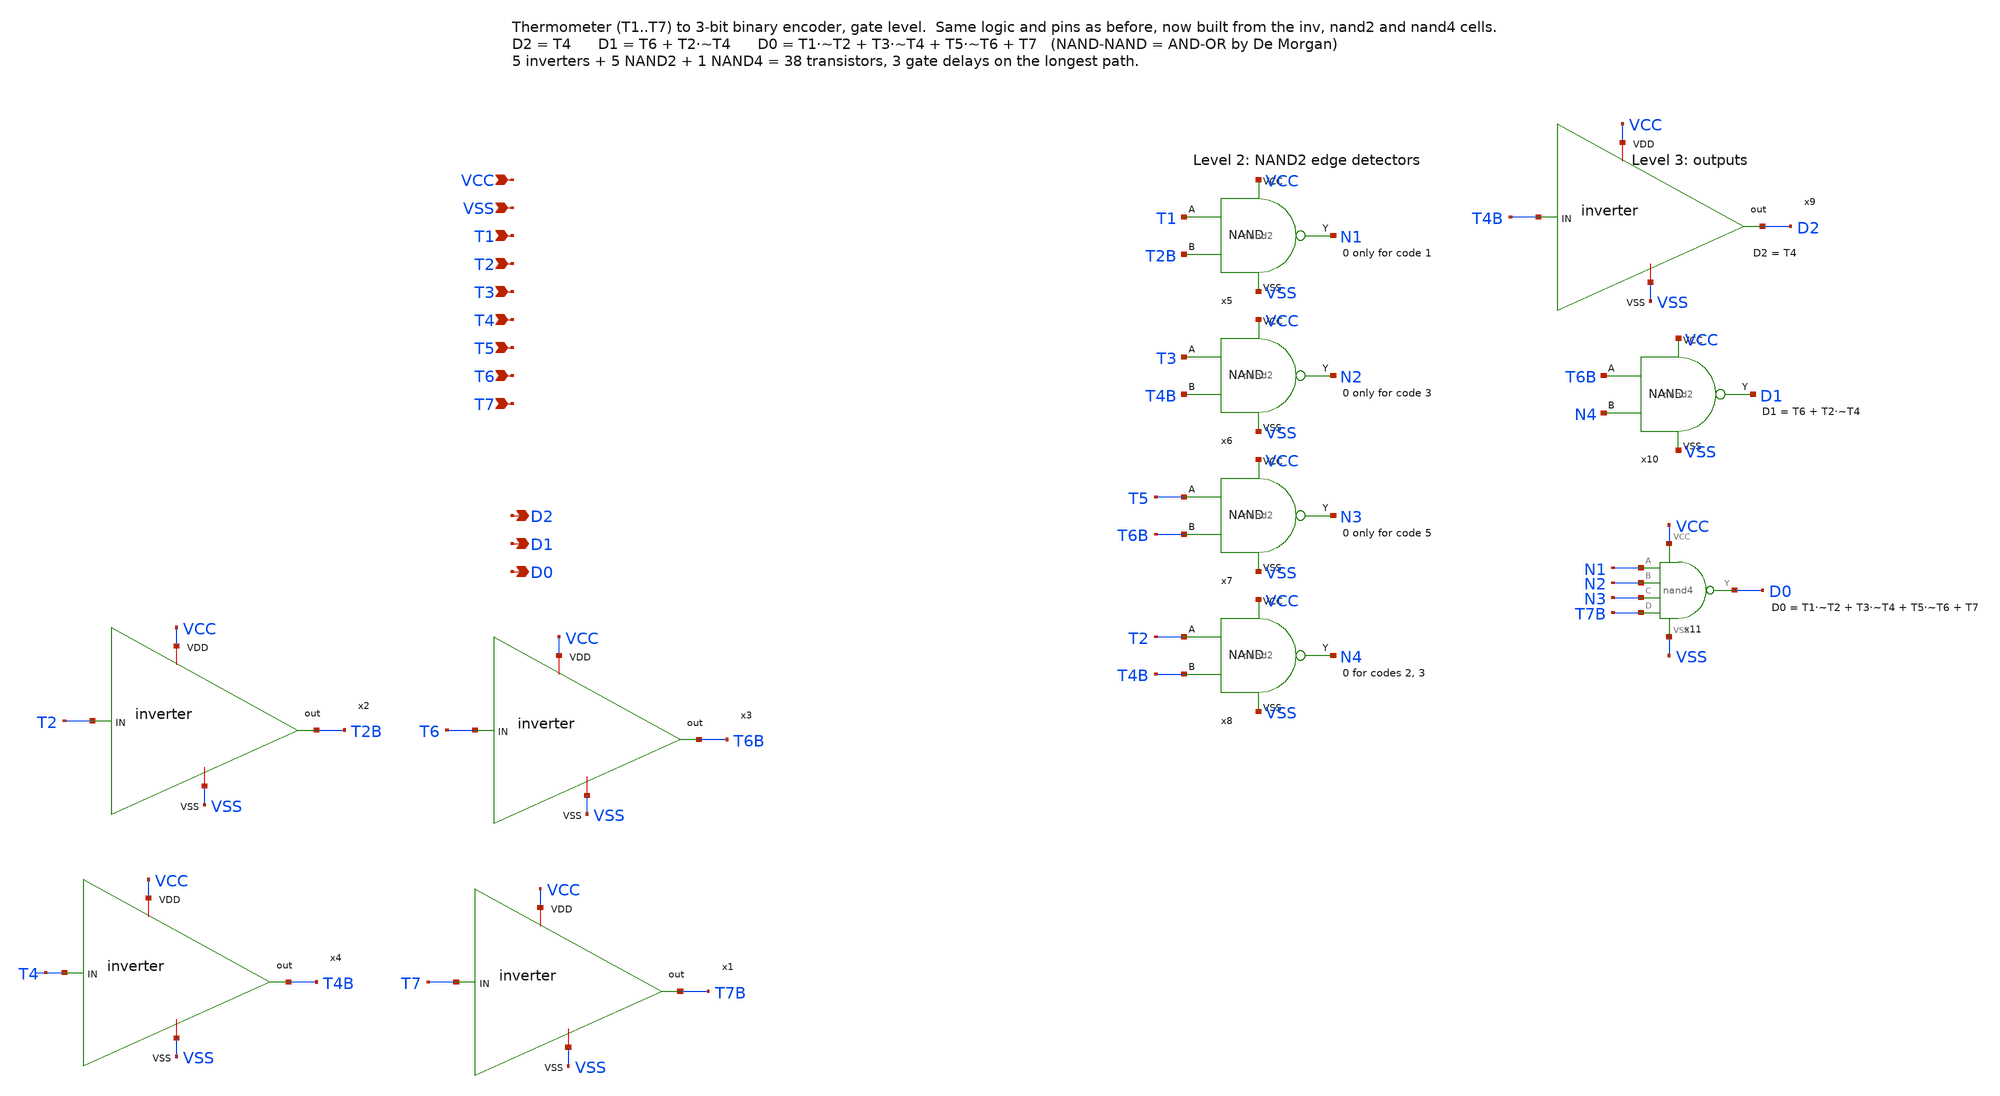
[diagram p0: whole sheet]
** sch_path: therm2bin3.sch
**.subckt therm2bin3 VCC VSS T1 T2 T3 T4 T5 T6 T7 D2 D1 D0
*.ipin VCC
*.ipin VSS
*.ipin T1
*.ipin T2
*.ipin T3
*.ipin T4
*.ipin T5
*.ipin T6
*.ipin T7
*.opin D2
*.opin D1
*.opin D0
x3 VCC T6 T6B VSS inverter
x5 T1 T2B N1 VCC VSS nand2
x6 T3 T4B N2 VCC VSS nand2
x7 T5 T6B N3 VCC VSS nand2
x8 T2 T4B N4 VCC VSS nand2
x9 VCC T4B D2 VSS inverter
x10 T6B N4 D1 VCC VSS nand2
x11 VCC VSS N1 N2 N3 T7B D0 nand4
x1 VCC T7 T7B VSS inverter
x2 VCC T2 T2B VSS inverter
x4 VCC T4 T4B VSS inverter
**.ends

* expanding   symbol:  /home/ttuser/Documents/ADCAnalogDesign/inverter.sym # of pins=4
** sym_path: inverter.sym
** sch_path: inverter.sch
.subckt inverter VDD IN out VSS
*.ipin IN
*.opin out
*.iopin VDD
*.iopin VSS
XM3 out IN VDD VDD sky130_fd_pr__pfet_01v8 L=0.15 W=1 nf=1 ad='int((nf+1)/2) * W/nf * 0.29' as='int((nf+2)/2) * W/nf * 0.29'
+ pd='2*int((nf+1)/2) * (W/nf + 0.29)' ps='2*int((nf+2)/2) * (W/nf + 0.29)' nrd='0.29 / W' nrs='0.29 / W'
+ sa=0 sb=0 sd=0 mult=1 m=1
XM2 out IN VSS VSS sky130_fd_pr__nfet_01v8 L=0.15 W=1 nf=1 ad='int((nf+1)/2) * W/nf * 0.29' as='int((nf+2)/2) * W/nf * 0.29'
+ pd='2*int((nf+1)/2) * (W/nf + 0.29)' ps='2*int((nf+2)/2) * (W/nf + 0.29)' nrd='0.29 / W' nrs='0.29 / W'
+ sa=0 sb=0 sd=0 mult=1 m=1
.ends


* expanding   symbol:  /home/ttuser/Documents/ADCAnalogDesign/nand2.sym # of pins=5
** sym_path: nand2.sym
** sch_path: nand2.sch
.subckt nand2 A B Y VCC VSS
*.ipin A
*.ipin B
*.opin Y
*.iopin VCC
*.iopin VSS
XM1 Y A VCC VCC sky130_fd_pr__pfet_01v8 L=0.15 W=2 nf=1 ad='int((nf+1)/2) * W/nf * 0.29' as='int((nf+2)/2) * W/nf * 0.29'
+ pd='2*int((nf+1)/2) * (W/nf + 0.29)' ps='2*int((nf+2)/2) * (W/nf + 0.29)' nrd='0.29 / W' nrs='0.29 / W'
+ sa=0 sb=0 sd=0 mult=1 m=1
XM2 Y B VCC VCC sky130_fd_pr__pfet_01v8 L=0.15 W=2 nf=1 ad='int((nf+1)/2) * W/nf * 0.29' as='int((nf+2)/2) * W/nf * 0.29'
+ pd='2*int((nf+1)/2) * (W/nf + 0.29)' ps='2*int((nf+2)/2) * (W/nf + 0.29)' nrd='0.29 / W' nrs='0.29 / W'
+ sa=0 sb=0 sd=0 mult=1 m=1
XM3 Y A N1 VSS sky130_fd_pr__nfet_01v8 L=0.15 W=2 nf=1 ad='int((nf+1)/2) * W/nf * 0.29' as='int((nf+2)/2) * W/nf * 0.29'
+ pd='2*int((nf+1)/2) * (W/nf + 0.29)' ps='2*int((nf+2)/2) * (W/nf + 0.29)' nrd='0.29 / W' nrs='0.29 / W'
+ sa=0 sb=0 sd=0 mult=1 m=1
XM4 N1 B VSS VSS sky130_fd_pr__nfet_01v8 L=0.15 W=2 nf=1 ad='int((nf+1)/2) * W/nf * 0.29' as='int((nf+2)/2) * W/nf * 0.29'
+ pd='2*int((nf+1)/2) * (W/nf + 0.29)' ps='2*int((nf+2)/2) * (W/nf + 0.29)' nrd='0.29 / W' nrs='0.29 / W'
+ sa=0 sb=0 sd=0 mult=1 m=1
.ends


* expanding   symbol:  /home/ttuser/Documents/ADCAnalogDesign/nand4.sym # of pins=7
** sym_path: nand4.sym
** sch_path: nand4.sch
.subckt nand4 VCC VSS A B C D Y
*.ipin VCC
*.ipin VSS
*.ipin A
*.ipin B
*.ipin C
*.ipin D
*.opin Y
XM1 Y A VCC VCC sky130_fd_pr__pfet_01v8 L=0.15 W=2 nf=1 ad='int((nf+1)/2) * W/nf * 0.29' as='int((nf+2)/2) * W/nf * 0.29'
+ pd='2*int((nf+1)/2) * (W/nf + 0.29)' ps='2*int((nf+2)/2) * (W/nf + 0.29)' nrd='0.29 / W' nrs='0.29 / W'
+ sa=0 sb=0 sd=0 mult=1 m=1
XM2 Y B VCC VCC sky130_fd_pr__pfet_01v8 L=0.15 W=2 nf=1 ad='int((nf+1)/2) * W/nf * 0.29' as='int((nf+2)/2) * W/nf * 0.29'
+ pd='2*int((nf+1)/2) * (W/nf + 0.29)' ps='2*int((nf+2)/2) * (W/nf + 0.29)' nrd='0.29 / W' nrs='0.29 / W'
+ sa=0 sb=0 sd=0 mult=1 m=1
XM3 Y C VCC VCC sky130_fd_pr__pfet_01v8 L=0.15 W=2 nf=1 ad='int((nf+1)/2) * W/nf * 0.29' as='int((nf+2)/2) * W/nf * 0.29'
+ pd='2*int((nf+1)/2) * (W/nf + 0.29)' ps='2*int((nf+2)/2) * (W/nf + 0.29)' nrd='0.29 / W' nrs='0.29 / W'
+ sa=0 sb=0 sd=0 mult=1 m=1
XM4 Y D VCC VCC sky130_fd_pr__pfet_01v8 L=0.15 W=2 nf=1 ad='int((nf+1)/2) * W/nf * 0.29' as='int((nf+2)/2) * W/nf * 0.29'
+ pd='2*int((nf+1)/2) * (W/nf + 0.29)' ps='2*int((nf+2)/2) * (W/nf + 0.29)' nrd='0.29 / W' nrs='0.29 / W'
+ sa=0 sb=0 sd=0 mult=1 m=1
XM5 Y A n1 VSS sky130_fd_pr__nfet_01v8 L=0.15 W=4 nf=1 ad='int((nf+1)/2) * W/nf * 0.29' as='int((nf+2)/2) * W/nf * 0.29'
+ pd='2*int((nf+1)/2) * (W/nf + 0.29)' ps='2*int((nf+2)/2) * (W/nf + 0.29)' nrd='0.29 / W' nrs='0.29 / W'
+ sa=0 sb=0 sd=0 mult=1 m=1
XM6 n1 B n2 VSS sky130_fd_pr__nfet_01v8 L=0.15 W=4 nf=1 ad='int((nf+1)/2) * W/nf * 0.29' as='int((nf+2)/2) * W/nf * 0.29'
+ pd='2*int((nf+1)/2) * (W/nf + 0.29)' ps='2*int((nf+2)/2) * (W/nf + 0.29)' nrd='0.29 / W' nrs='0.29 / W'
+ sa=0 sb=0 sd=0 mult=1 m=1
XM7 n2 C n3 VSS sky130_fd_pr__nfet_01v8 L=0.15 W=4 nf=1 ad='int((nf+1)/2) * W/nf * 0.29' as='int((nf+2)/2) * W/nf * 0.29'
+ pd='2*int((nf+1)/2) * (W/nf + 0.29)' ps='2*int((nf+2)/2) * (W/nf + 0.29)' nrd='0.29 / W' nrs='0.29 / W'
+ sa=0 sb=0 sd=0 mult=1 m=1
XM8 n3 D VSS VSS sky130_fd_pr__nfet_01v8 L=0.15 W=4 nf=1 ad='int((nf+1)/2) * W/nf * 0.29' as='int((nf+2)/2) * W/nf * 0.29'
+ pd='2*int((nf+1)/2) * (W/nf + 0.29)' ps='2*int((nf+2)/2) * (W/nf + 0.29)' nrd='0.29 / W' nrs='0.29 / W'
+ sa=0 sb=0 sd=0 mult=1 m=1
.ends

.end
